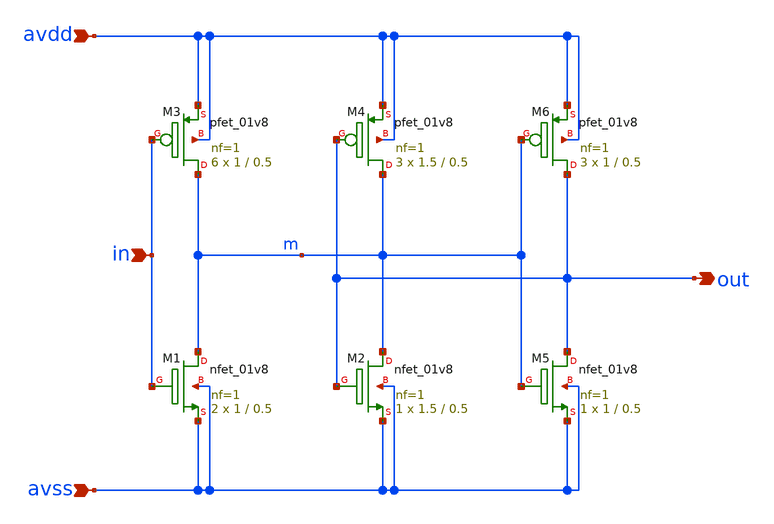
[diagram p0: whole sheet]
** sch_path: xschem/schmitt_trigger.sch
**.subckt schmitt_trigger avdd avss out in
*.ipin avdd
*.ipin avss
*.opin out
*.ipin in
XM1 m in avss avss sky130_fd_pr__nfet_01v8 L=0.5 W=1 nf=1 ad='int((nf+1)/2) * W/nf * 0.29' as='int((nf+2)/2) * W/nf * 0.29'
+ pd='2*int((nf+1)/2) * (W/nf + 0.29)' ps='2*int((nf+2)/2) * (W/nf + 0.29)' nrd='0.29 / W' nrs='0.29 / W'
+ sa=0 sb=0 sd=0 mult=2 m=2
XM3 m in avdd avdd sky130_fd_pr__pfet_01v8 L=0.5 W=1 nf=1 ad='int((nf+1)/2) * W/nf * 0.29' as='int((nf+2)/2) * W/nf * 0.29'
+ pd='2*int((nf+1)/2) * (W/nf + 0.29)' ps='2*int((nf+2)/2) * (W/nf + 0.29)' nrd='0.29 / W' nrs='0.29 / W'
+ sa=0 sb=0 sd=0 mult=6 m=6
XM2 m out avss avss sky130_fd_pr__nfet_01v8 L=0.5 W=1.5 nf=1 ad='int((nf+1)/2) * W/nf * 0.29' as='int((nf+2)/2) * W/nf * 0.29'
+ pd='2*int((nf+1)/2) * (W/nf + 0.29)' ps='2*int((nf+2)/2) * (W/nf + 0.29)' nrd='0.29 / W' nrs='0.29 / W'
+ sa=0 sb=0 sd=0 mult=1 m=1
XM4 m out avdd avdd sky130_fd_pr__pfet_01v8 L=0.5 W=1.5 nf=1 ad='int((nf+1)/2) * W/nf * 0.29' as='int((nf+2)/2) * W/nf * 0.29'
+ pd='2*int((nf+1)/2) * (W/nf + 0.29)' ps='2*int((nf+2)/2) * (W/nf + 0.29)' nrd='0.29 / W' nrs='0.29 / W'
+ sa=0 sb=0 sd=0 mult=3 m=3
XM5 out m avss avss sky130_fd_pr__nfet_01v8 L=0.5 W=1 nf=1 ad='int((nf+1)/2) * W/nf * 0.29' as='int((nf+2)/2) * W/nf * 0.29'
+ pd='2*int((nf+1)/2) * (W/nf + 0.29)' ps='2*int((nf+2)/2) * (W/nf + 0.29)' nrd='0.29 / W' nrs='0.29 / W'
+ sa=0 sb=0 sd=0 mult=1 m=1
XM6 out m avdd avdd sky130_fd_pr__pfet_01v8 L=0.5 W=1 nf=1 ad='int((nf+1)/2) * W/nf * 0.29' as='int((nf+2)/2) * W/nf * 0.29'
+ pd='2*int((nf+1)/2) * (W/nf + 0.29)' ps='2*int((nf+2)/2) * (W/nf + 0.29)' nrd='0.29 / W' nrs='0.29 / W'
+ sa=0 sb=0 sd=0 mult=3 m=3
**.ends
.end
